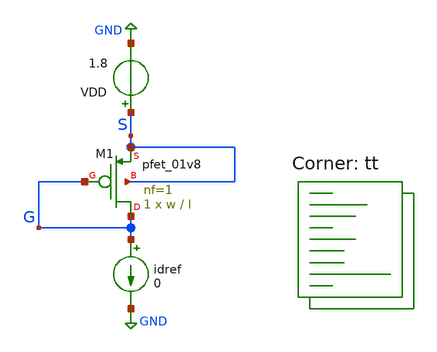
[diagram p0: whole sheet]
** sch_path: characterisationPMOS.sch
**.subckt characterisationPMOS
idref G GND 0
VDD S GND 1.8
XM1 G G S S sky130_fd_pr__pfet_01v8 L=l W=w nf=1 ad='int((nf+1)/2) * W/nf * 0.29' as='int((nf+2)/2) * W/nf * 0.29'
+ pd='2*int((nf+1)/2) * (W/nf + 0.29)' ps='2*int((nf+2)/2) * (W/nf + 0.29)' nrd='0.29 / W' nrs='0.29 / W'
+ sa=0 sb=0 sd=0 mult=1 m=1
**** begin user architecture code


.param l=0.28
.param w=1.2
.op
.save all
.control

let n_idx = 2000
let start_iref =0.01u
let stop_iref = 800u
let delta_iref = (stop_iref - start_iref) / n_idx
let iref_act = start_iref

let vgs = unitvec(n_idx)
let gms = unitvec(n_idx)
let ids = unitvec(n_idx)
let idsw = unitvec(n_idx)
let gdss=unitvec(n_idx)
let gdssw=unitvec(n_idx)

let idxs = 0
let idx = idxs
let w = 1.2u
*loop
while iref_act le stop_iref
  alter idref iref_act
  run
  let gms[idx] = @m.xm1.msky130_fd_pr__pfet_01v8[gm]
  let ids[idx] = -(@m.xm1.msky130_fd_pr__pfet_01v8[id])
  let idsw[idx]= (-@m.xm1.msky130_fd_pr__pfet_01v8[id])/w
  let gdss[idx] = @m.xm1.msky130_fd_pr__pfet_01v8[gds]
  let gdssw[idx] = @m.xm1.msky130_fd_pr__pfet_01v8[gds]/w
  let vgs[idx] = v(G)-v(S)
  let iref_act = iref_act + delta_iref
  let idxs = idx + 1
  let idx = idxs
end

settype voltage vgs
settype current ids
setscale ids
*plot gms/gdss vs gms/ids
plot gms/ids vs idsw
*plot gms/gdss vs idsw
*plot gdssw vs idsw
*plot vgs vs idsw
plot gdss/ids vs idsw
.endc
.end


.lib $::SKYWATER_MODELS/sky130.lib.spice tt
**** end user architecture code
**.ends
.GLOBAL GND
.end
